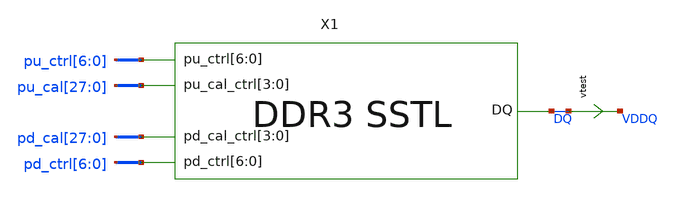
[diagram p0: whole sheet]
** sch_path: schem/sstl_res_tb.sch
* Copyright 2021 Stefan Frederik Schippers
* Licensed under the Apache License, Version 2.0 (the "License");
* you may not use this file except in compliance with the License.
* You may obtain a copy of the License at
* https://www.apache.org/licenses/LICENSE-2.0
* Unless required by applicable law or agreed to in writing, software
* distributed under the License is distributed on an "AS IS" BASIS,
* WITHOUT WARRANTIES OR CONDITIONS OF ANY KIND, either express or implied.
* See the License for the specific language governing permissions and
* limitations under the License.
**.subckt sstl_res_tb
vtest DQ VDDQ 0
.save i(vtest)
X1 DQ pd_ctrl[6] pd_ctrl[5] pd_ctrl[4] pd_ctrl[3] pd_ctrl[2] pd_ctrl[1] pd_ctrl[0] pu_ctrl[6]
+ pu_ctrl[5] pu_ctrl[4] pu_ctrl[3] pu_ctrl[2] pu_ctrl[1] pu_ctrl[0] pd_cal[27] pd_cal[26] pd_cal[25] pd_cal[24]
+ pu_cal[27] pu_cal[26] pu_cal[25] pu_cal[24] SSTL
**** begin user architecture code
 ** Local library links to pdk
.lib ./sky130/libs/SED_process_SED_lib.spice SED_process_SED
.include $::SKYWATER_STDCELLS/sky130_fd_sc_hd.spice

**** end user architecture code
**.ends

* expanding   symbol:  SSTL.sym # of pins=5
** sym_path: schem/SSTL.sym
** sch_path: schem/SSTL.sch
.subckt SSTL DQ pd_ctrl[6] pd_ctrl[5] pd_ctrl[4] pd_ctrl[3] pd_ctrl[2] pd_ctrl[1] pd_ctrl[0]
+ pu_ctrl[6] pu_ctrl[5] pu_ctrl[4] pu_ctrl[3] pu_ctrl[2] pu_ctrl[1] pu_ctrl[0] pd_cal_ctrl[3] pd_cal_ctrl[2]
+ pd_cal_ctrl[1] pd_cal_ctrl[0] pu_cal_ctrl[3] pu_cal_ctrl[2] pu_cal_ctrl[1] pu_cal_ctrl[0]
*.iopin DQ
*.ipin pu_cal_ctrl[3],pu_cal_ctrl[2],pu_cal_ctrl[1],pu_cal_ctrl[0]
*.ipin pd_cal_ctrl[3],pd_cal_ctrl[2],pd_cal_ctrl[1],pd_cal_ctrl[0]
*.ipin pu_ctrl[6],pu_ctrl[5],pu_ctrl[4],pu_ctrl[3],pu_ctrl[2],pu_ctrl[1],pu_ctrl[0]
*.ipin pd_ctrl[6],pd_ctrl[5],pd_ctrl[4],pd_ctrl[3],pd_ctrl[2],pd_ctrl[1],pd_ctrl[0]
X1 DQ n_pu_ctrl[6] n_pu_cal_ctrl[3] n_pu_cal_ctrl[2] n_pu_cal_ctrl[1] n_pu_cal_ctrl[0] p-leg
X2 DQ pd_ctrl_buff[6] pd_cal_ctrl[3] pd_cal_ctrl[2] pd_cal_ctrl[1] pd_cal_ctrl[0] n-leg
X3 DQ n_pu_ctrl[5] n_pu_cal_ctrl[3] n_pu_cal_ctrl[2] n_pu_cal_ctrl[1] n_pu_cal_ctrl[0] p-leg
X4 DQ pd_ctrl_buff[5] pd_cal_ctrl[3] pd_cal_ctrl[2] pd_cal_ctrl[1] pd_cal_ctrl[0] n-leg
X5 DQ n_pu_ctrl[4] n_pu_cal_ctrl[3] n_pu_cal_ctrl[2] n_pu_cal_ctrl[1] n_pu_cal_ctrl[0] p-leg
X6 DQ pd_ctrl_buff[4] pd_cal_ctrl[3] pd_cal_ctrl[2] pd_cal_ctrl[1] pd_cal_ctrl[0] n-leg
X7 DQ n_pu_ctrl[3] n_pu_cal_ctrl[3] n_pu_cal_ctrl[2] n_pu_cal_ctrl[1] n_pu_cal_ctrl[0] p-leg
X8 DQ pd_ctrl_buff[3] pd_cal_ctrl[3] pd_cal_ctrl[2] pd_cal_ctrl[1] pd_cal_ctrl[0] n-leg
X9 DQ n_pu_ctrl[2] n_pu_cal_ctrl[3] n_pu_cal_ctrl[2] n_pu_cal_ctrl[1] n_pu_cal_ctrl[0] p-leg
X10 DQ pd_ctrl_buff[2] pd_cal_ctrl[3] pd_cal_ctrl[2] pd_cal_ctrl[1] pd_cal_ctrl[0] n-leg
X11 DQ n_pu_ctrl[1] n_pu_cal_ctrl[3] n_pu_cal_ctrl[2] n_pu_cal_ctrl[1] n_pu_cal_ctrl[0] p-leg
X12 DQ pd_ctrl_buff[1] pd_cal_ctrl[3] pd_cal_ctrl[2] pd_cal_ctrl[1] pd_cal_ctrl[0] n-leg
X13 DQ n_pu_ctrl[0] n_pu_cal_ctrl[3] n_pu_cal_ctrl[2] n_pu_cal_ctrl[1] n_pu_cal_ctrl[0] p-leg
X14 DQ pd_ctrl_buff[0] pd_cal_ctrl[3] pd_cal_ctrl[2] pd_cal_ctrl[1] pd_cal_ctrl[0] n-leg
xpd_buff_4[6] pdc2[6] VGND VNB VPB VPWR pdc4[6] sky130_fd_sc_hd__clkinv_4
xpd_buff_4[5] pdc2[5] VGND VNB VPB VPWR pdc4[5] sky130_fd_sc_hd__clkinv_4
xpd_buff_4[4] pdc2[4] VGND VNB VPB VPWR pdc4[4] sky130_fd_sc_hd__clkinv_4
xpd_buff_4[3] pdc2[3] VGND VNB VPB VPWR pdc4[3] sky130_fd_sc_hd__clkinv_4
xpd_buff_4[2] pdc2[2] VGND VNB VPB VPWR pdc4[2] sky130_fd_sc_hd__clkinv_4
xpd_buff_4[1] pdc2[1] VGND VNB VPB VPWR pdc4[1] sky130_fd_sc_hd__clkinv_4
xpd_buff_4[0] pdc2[0] VGND VNB VPB VPWR pdc4[0] sky130_fd_sc_hd__clkinv_4
xpd_buff_6[6] pdc4[6] VGND VNB VPB VPWR pd_ctrl_buff[6] sky130_fd_sc_hd__clkbuf_8
xpd_buff_6[5] pdc4[5] VGND VNB VPB VPWR pd_ctrl_buff[5] sky130_fd_sc_hd__clkbuf_8
xpd_buff_6[4] pdc4[4] VGND VNB VPB VPWR pd_ctrl_buff[4] sky130_fd_sc_hd__clkbuf_8
xpd_buff_6[3] pdc4[3] VGND VNB VPB VPWR pd_ctrl_buff[3] sky130_fd_sc_hd__clkbuf_8
xpd_buff_6[2] pdc4[2] VGND VNB VPB VPWR pd_ctrl_buff[2] sky130_fd_sc_hd__clkbuf_8
xpd_buff_6[1] pdc4[1] VGND VNB VPB VPWR pd_ctrl_buff[1] sky130_fd_sc_hd__clkbuf_8
xpd_buff_6[0] pdc4[0] VGND VNB VPB VPWR pd_ctrl_buff[0] sky130_fd_sc_hd__clkbuf_8
xpu_buff_4[6] pu_ctrl[6] VGND VNB VPB VPWR puc4[6] sky130_fd_sc_hd__clkbuf_16
xpu_buff_4[5] pu_ctrl[5] VGND VNB VPB VPWR puc4[5] sky130_fd_sc_hd__clkbuf_16
xpu_buff_4[4] pu_ctrl[4] VGND VNB VPB VPWR puc4[4] sky130_fd_sc_hd__clkbuf_16
xpu_buff_4[3] pu_ctrl[3] VGND VNB VPB VPWR puc4[3] sky130_fd_sc_hd__clkbuf_16
xpu_buff_4[2] pu_ctrl[2] VGND VNB VPB VPWR puc4[2] sky130_fd_sc_hd__clkbuf_16
xpu_buff_4[1] pu_ctrl[1] VGND VNB VPB VPWR puc4[1] sky130_fd_sc_hd__clkbuf_16
xpu_buff_4[0] pu_ctrl[0] VGND VNB VPB VPWR puc4[0] sky130_fd_sc_hd__clkbuf_16
xpu_buff_6[6] puc4[6] VGND VNB VPB VPWR n_pu_ctrl[6] sky130_fd_sc_hd__clkinv_16
xpu_buff_6[5] puc4[5] VGND VNB VPB VPWR n_pu_ctrl[5] sky130_fd_sc_hd__clkinv_16
xpu_buff_6[4] puc4[4] VGND VNB VPB VPWR n_pu_ctrl[4] sky130_fd_sc_hd__clkinv_16
xpu_buff_6[3] puc4[3] VGND VNB VPB VPWR n_pu_ctrl[3] sky130_fd_sc_hd__clkinv_16
xpu_buff_6[2] puc4[2] VGND VNB VPB VPWR n_pu_ctrl[2] sky130_fd_sc_hd__clkinv_16
xpu_buff_6[1] puc4[1] VGND VNB VPB VPWR n_pu_ctrl[1] sky130_fd_sc_hd__clkinv_16
xpu_buff_6[0] puc4[0] VGND VNB VPB VPWR n_pu_ctrl[0] sky130_fd_sc_hd__clkinv_16
xpu_cal_inv[3] pu_cal_ctrl[3] VGND VNB VPB VPWR n_pu_cal_ctrl[3] sky130_fd_sc_hd__inv_1
xpu_cal_inv[2] pu_cal_ctrl[2] VGND VNB VPB VPWR n_pu_cal_ctrl[2] sky130_fd_sc_hd__inv_1
xpu_cal_inv[1] pu_cal_ctrl[1] VGND VNB VPB VPWR n_pu_cal_ctrl[1] sky130_fd_sc_hd__inv_1
xpu_cal_inv[0] pu_cal_ctrl[0] VGND VNB VPB VPWR n_pu_cal_ctrl[0] sky130_fd_sc_hd__inv_1
V1 VDD VPWR 0
V2 VGND GND 0
V3 VDD VPB 0
V4 VNB GND 0
Vpd_ctrl_0 v_pd_ctrl_0 pd_ctrl_buff[6] 0
Vpd_ctrl_1 v_pu_ctrl_0 n_pu_ctrl[6] 0
xpu_buff_2[6] puc4[6] VGND VNB VPB VPWR n_pu_ctrl[6] sky130_fd_sc_hd__clkinv_16
xpu_buff_2[5] puc4[5] VGND VNB VPB VPWR n_pu_ctrl[5] sky130_fd_sc_hd__clkinv_16
xpu_buff_2[4] puc4[4] VGND VNB VPB VPWR n_pu_ctrl[4] sky130_fd_sc_hd__clkinv_16
xpu_buff_2[3] puc4[3] VGND VNB VPB VPWR n_pu_ctrl[3] sky130_fd_sc_hd__clkinv_16
xpu_buff_2[2] puc4[2] VGND VNB VPB VPWR n_pu_ctrl[2] sky130_fd_sc_hd__clkinv_16
xpu_buff_2[1] puc4[1] VGND VNB VPB VPWR n_pu_ctrl[1] sky130_fd_sc_hd__clkinv_16
xpu_buff_2[0] puc4[0] VGND VNB VPB VPWR n_pu_ctrl[0] sky130_fd_sc_hd__clkinv_16
xpd_buff_1[6] pd_ctrl[6] VGND VNB VPB VPWR pdc2[6] sky130_fd_sc_hd__clkinv_4
xpd_buff_1[5] pd_ctrl[5] VGND VNB VPB VPWR pdc2[5] sky130_fd_sc_hd__clkinv_4
xpd_buff_1[4] pd_ctrl[4] VGND VNB VPB VPWR pdc2[4] sky130_fd_sc_hd__clkinv_4
xpd_buff_1[3] pd_ctrl[3] VGND VNB VPB VPWR pdc2[3] sky130_fd_sc_hd__clkinv_4
xpd_buff_1[2] pd_ctrl[2] VGND VNB VPB VPWR pdc2[2] sky130_fd_sc_hd__clkinv_4
xpd_buff_1[1] pd_ctrl[1] VGND VNB VPB VPWR pdc2[1] sky130_fd_sc_hd__clkinv_4
xpd_buff_1[0] pd_ctrl[0] VGND VNB VPB VPWR pdc2[0] sky130_fd_sc_hd__clkinv_4
xpu_buff_1[6] puc4[6] VGND VNB VPB VPWR n_pu_ctrl[6] sky130_fd_sc_hd__clkinv_16
xpu_buff_1[5] puc4[5] VGND VNB VPB VPWR n_pu_ctrl[5] sky130_fd_sc_hd__clkinv_16
xpu_buff_1[4] puc4[4] VGND VNB VPB VPWR n_pu_ctrl[4] sky130_fd_sc_hd__clkinv_16
xpu_buff_1[3] puc4[3] VGND VNB VPB VPWR n_pu_ctrl[3] sky130_fd_sc_hd__clkinv_16
xpu_buff_1[2] puc4[2] VGND VNB VPB VPWR n_pu_ctrl[2] sky130_fd_sc_hd__clkinv_16
xpu_buff_1[1] puc4[1] VGND VNB VPB VPWR n_pu_ctrl[1] sky130_fd_sc_hd__clkinv_16
xpu_buff_1[0] puc4[0] VGND VNB VPB VPWR n_pu_ctrl[0] sky130_fd_sc_hd__clkinv_16
.ends


* expanding   symbol:  p-leg.sym # of pins=3
** sym_path: schem/p-leg.sym
** sch_path: schem/p-leg.sch
.subckt p-leg DQ n_pu_ctrl n_cal_ctrl[3] n_cal_ctrl[2] n_cal_ctrl[1] n_cal_ctrl[0]
*.ipin n_cal_ctrl[3],n_cal_ctrl[2],n_cal_ctrl[1],n_cal_ctrl[0]
*.ipin n_pu_ctrl
*.iopin DQ
XR1 DQ net1 sky130_fd_pr__res_generic_po W=0.33 L=1.8 m=1
XMpullup net1 n_pu_ctrl VDD VDD sky130_fd_pr__pfet_01v8_lvt L=0.35 W=1 nf=1 ad='int((nf+1)/2) * W/nf * 0.29'
+ as='int((nf+2)/2) * W/nf * 0.29' pd='2*int((nf+1)/2) * (W/nf + 0.29)' ps='2*int((nf+2)/2) * (W/nf + 0.29)'
+ nrd='0.29 / W' nrs='0.29 / W' sa=0 sb=0 sd=0 mult=128 m=128
XMctrltot VDD n_cal_ctrl[0] VDD VDD sky130_fd_pr__pfet_01v8_lvt L=0.35 W=1 nf=1 ad='int((nf+1)/2) * W/nf * 0.29'
+ as='int((nf+2)/2) * W/nf * 0.29' pd='2*int((nf+1)/2) * (W/nf + 0.29)' ps='2*int((nf+2)/2) * (W/nf + 0.29)'
+ nrd='0.29 / W' nrs='0.29 / W' sa=0 sb=0 sd=0 mult=120 m=120
XMctrl0 DQ n_cal_ctrl[0] net1 VDD sky130_fd_pr__pfet_01v8_lvt L=0.35 W=1 nf=1 ad='int((nf+1)/2) * W/nf * 0.29'
+ as='int((nf+2)/2) * W/nf * 0.29' pd='2*int((nf+1)/2) * (W/nf + 0.29)' ps='2*int((nf+2)/2) * (W/nf + 0.29)'
+ nrd='0.29 / W' nrs='0.29 / W' sa=0 sb=0 sd=0 mult=48 m=48
XMctrl1 DQ n_cal_ctrl[1] net1 VDD sky130_fd_pr__pfet_01v8_lvt L=0.35 W=1 nf=1 ad='int((nf+1)/2) * W/nf * 0.29'
+ as='int((nf+2)/2) * W/nf * 0.29' pd='2*int((nf+1)/2) * (W/nf + 0.29)' ps='2*int((nf+2)/2) * (W/nf + 0.29)'
+ nrd='0.29 / W' nrs='0.29 / W' sa=0 sb=0 sd=0 mult=16 m=16
XMctrl2 DQ n_cal_ctrl[2] net1 VDD sky130_fd_pr__pfet_01v8_lvt L=0.35 W=1 nf=1 ad='int((nf+1)/2) * W/nf * 0.29'
+ as='int((nf+2)/2) * W/nf * 0.29' pd='2*int((nf+1)/2) * (W/nf + 0.29)' ps='2*int((nf+2)/2) * (W/nf + 0.29)'
+ nrd='0.29 / W' nrs='0.29 / W' sa=0 sb=0 sd=0 mult=8 m=8
XMctrl3 DQ n_cal_ctrl[3] net1 VDD sky130_fd_pr__pfet_01v8_lvt L=0.35 W=1 nf=1 ad='int((nf+1)/2) * W/nf * 0.29'
+ as='int((nf+2)/2) * W/nf * 0.29' pd='2*int((nf+1)/2) * (W/nf + 0.29)' ps='2*int((nf+2)/2) * (W/nf + 0.29)'
+ nrd='0.29 / W' nrs='0.29 / W' sa=0 sb=0 sd=0 mult=4 m=4
.ends


* expanding   symbol:  n-leg.sym # of pins=3
** sym_path: schem/n-leg.sym
** sch_path: schem/n-leg.sch
.subckt n-leg DQ pd_ctrl cal_ctrl[3] cal_ctrl[2] cal_ctrl[1] cal_ctrl[0]
*.iopin DQ
*.ipin pd_ctrl
*.ipin cal_ctrl[3],cal_ctrl[2],cal_ctrl[1],cal_ctrl[0]
XR1 vpulldown DQ sky130_fd_pr__res_generic_po W=0.33 L=1.7 m=1
Xn1 vpulldown pd_ctrl GND GND sky130_fd_pr__nfet_01v8 L=0.15 W=0.65 nf=1 ad='int((nf+1)/2) * W/nf * 0.29'
+ as='int((nf+2)/2) * W/nf * 0.29' pd='2*int((nf+1)/2) * (W/nf + 0.29)' ps='2*int((nf+2)/2) * (W/nf + 0.29)'
+ nrd='0.29 / W' nrs='0.29 / W' sa=0 sb=0 sd=0 mult=48 m=48
Xnctrl0 DQ cal_ctrl[0] vpulldown GND sky130_fd_pr__nfet_01v8 L=0.15 W=0.65 nf=1 ad='int((nf+1)/2) * W/nf * 0.29'
+ as='int((nf+2)/2) * W/nf * 0.29' pd='2*int((nf+1)/2) * (W/nf + 0.29)' ps='2*int((nf+2)/2) * (W/nf + 0.29)'
+ nrd='0.29 / W' nrs='0.29 / W' sa=0 sb=0 sd=0 mult=6 m=6
Xnctrl1 DQ cal_ctrl[1] vpulldown GND sky130_fd_pr__nfet_01v8 L=0.15 W=0.65 nf=1 ad='int((nf+1)/2) * W/nf * 0.29'
+ as='int((nf+2)/2) * W/nf * 0.29' pd='2*int((nf+1)/2) * (W/nf + 0.29)' ps='2*int((nf+2)/2) * (W/nf + 0.29)'
+ nrd='0.29 / W' nrs='0.29 / W' sa=0 sb=0 sd=0 mult=3 m=3
Xnctrl2 DQ cal_ctrl[2] vpulldown GND sky130_fd_pr__nfet_01v8 L=0.15 W=0.975 nf=1 ad='int((nf+1)/2) * W/nf * 0.29'
+ as='int((nf+2)/2) * W/nf * 0.29' pd='2*int((nf+1)/2) * (W/nf + 0.29)' ps='2*int((nf+2)/2) * (W/nf + 0.29)'
+ nrd='0.29 / W' nrs='0.29 / W' sa=0 sb=0 sd=0 mult=1 m=1
Xnctrl3 DQ cal_ctrl[3] vpulldown GND sky130_fd_pr__nfet_01v8 L=0.15 W=0.5 nf=1 ad='int((nf+1)/2) * W/nf * 0.29'
+ as='int((nf+2)/2) * W/nf * 0.29' pd='2*int((nf+1)/2) * (W/nf + 0.29)' ps='2*int((nf+2)/2) * (W/nf + 0.29)'
+ nrd='0.29 / W' nrs='0.29 / W' sa=0 sb=0 sd=0 mult=1 m=1
Xnctrl_tot GND GND GND GND sky130_fd_pr__nfet_01v8 L=0.15 W=0.65 nf=1 ad='int((nf+1)/2) * W/nf * 0.29'
+ as='int((nf+2)/2) * W/nf * 0.29' pd='2*int((nf+1)/2) * (W/nf + 0.29)' ps='2*int((nf+2)/2) * (W/nf + 0.29)'
+ nrd='0.29 / W' nrs='0.29 / W' sa=0 sb=0 sd=0 mult=11 m=11
.ends

.GLOBAL VDD
.GLOBAL GND
**** begin user architecture code


* power voltage
vvddq VDDQ 0 0
vvdd VDD 0 SED_vdd_SED

** CALIBRATION CONTROL **
* PULLUP
vpu_cal00 pu_cal[0] 0 SED_pucal00_SED
vpu_cal01 pu_cal[1] 0 SED_pucal01_SED
vpu_cal02 pu_cal[2] 0 SED_pucal02_SED
vpu_cal03 pu_cal[3] 0 SED_pucal03_SED
vpu_cal10 pu_cal[4] 0 SED_pucal10_SED
vpu_cal11 pu_cal[5] 0 SED_pucal11_SED
vpu_cal12 pu_cal[6] 0 SED_pucal12_SED
vpu_cal13 pu_cal[7] 0 SED_pucal13_SED
vpu_cal20 pu_cal[8] 0 SED_pucal20_SED
vpu_cal21 pu_cal[9] 0 SED_pucal21_SED
vpu_cal22 pu_cal[10] 0 SED_pucal22_SED
vpu_cal23 pu_cal[11] 0 SED_pucal23_SED
vpu_cal30 pu_cal[12] 0 SED_pucal30_SED
vpu_cal31 pu_cal[13] 0 SED_pucal31_SED
vpu_cal32 pu_cal[14] 0 SED_pucal32_SED
vpu_cal33 pu_cal[15] 0 SED_pucal33_SED
vpu_cal40 pu_cal[16] 0 SED_pucal40_SED
vpu_cal41 pu_cal[17] 0 SED_pucal41_SED
vpu_cal42 pu_cal[18] 0 SED_pucal42_SED
vpu_cal43 pu_cal[19] 0 SED_pucal43_SED
vpu_cal50 pu_cal[20] 0 SED_pucal50_SED
vpu_cal51 pu_cal[21] 0 SED_pucal51_SED
vpu_cal52 pu_cal[22] 0 SED_pucal52_SED
vpu_cal53 pu_cal[23] 0 SED_pucal53_SED
vpu_cal60 pu_cal[24] 0 SED_pucal60_SED
vpu_cal61 pu_cal[25] 0 SED_pucal61_SED
vpu_cal62 pu_cal[26] 0 SED_pucal62_SED
vpu_cal63 pu_cal[27] 0 SED_pucal63_SED
* PULLDOWN
vpd_cal00 pd_cal[0] 0 SED_pdcal00_SED
vpd_cal01 pd_cal[1] 0 SED_pdcal01_SED
vpd_cal02 pd_cal[2] 0 SED_pdcal02_SED
vpd_cal03 pd_cal[3] 0 SED_pdcal03_SED
vpd_cal10 pd_cal[4] 0 SED_pdcal10_SED
vpd_cal11 pd_cal[5] 0 SED_pdcal11_SED
vpd_cal12 pd_cal[6] 0 SED_pdcal12_SED
vpd_cal13 pd_cal[7] 0 SED_pdcal13_SED
vpd_cal20 pd_cal[8] 0 SED_pdcal20_SED
vpd_cal21 pd_cal[9] 0 SED_pdcal21_SED
vpd_cal22 pd_cal[10] 0 SED_pdcal22_SED
vpd_cal23 pd_cal[11] 0 SED_pdcal23_SED
vpd_cal30 pd_cal[12] 0 SED_pdcal30_SED
vpd_cal31 pd_cal[13] 0 SED_pdcal31_SED
vpd_cal32 pd_cal[14] 0 SED_pdcal32_SED
vpd_cal33 pd_cal[15] 0 SED_pdcal33_SED
vpd_cal40 pd_cal[16] 0 SED_pdcal40_SED
vpd_cal41 pd_cal[17] 0 SED_pdcal41_SED
vpd_cal42 pd_cal[18] 0 SED_pdcal42_SED
vpd_cal43 pd_cal[19] 0 SED_pdcal43_SED
vpd_cal50 pd_cal[20] 0 SED_pdcal50_SED
vpd_cal51 pd_cal[21] 0 SED_pdcal51_SED
vpd_cal52 pd_cal[22] 0 SED_pdcal52_SED
vpd_cal53 pd_cal[23] 0 SED_pdcal53_SED
vpd_cal60 pd_cal[24] 0 SED_pdcal60_SED
vpd_cal61 pd_cal[25] 0 SED_pdcal61_SED
vpd_cal62 pd_cal[26] 0 SED_pdcal62_SED
vpd_cal63 pd_cal[27] 0 SED_pdcal63_SED

** LEG ENABLE/DISABLE CONTROL
* PULLUP
vpu_ctrl0 pu_ctrl[0] 0 SED_puctrl0_SED
vpu_ctrl1 pu_ctrl[1] 0 SED_puctrl1_SED
vpu_ctrl2 pu_ctrl[2] 0 SED_puctrl2_SED
vpu_ctrl3 pu_ctrl[3] 0 SED_puctrl3_SED
vpu_ctrl4 pu_ctrl[4] 0 SED_puctrl4_SED
vpu_ctrl5 pu_ctrl[5] 0 SED_puctrl5_SED
vpu_ctrl6 pu_ctrl[6] 0 SED_puctrl6_SED
* PULLDOWN
vpd_ctrl0 pd_ctrl[0] 0 SED_pdctrl0_SED
vpd_ctrl1 pd_ctrl[1] 0 SED_pdctrl1_SED
vpd_ctrl2 pd_ctrl[2] 0 SED_pdctrl2_SED
vpd_ctrl3 pd_ctrl[3] 0 SED_pdctrl3_SED
vpd_ctrl4 pd_ctrl[4] 0 SED_pdctrl4_SED
vpd_ctrl5 pd_ctrl[5] 0 SED_pdctrl5_SED
vpd_ctrl6 pd_ctrl[6] 0 SED_pdctrl6_SED


.control
set num_threads=1
save all
set temp=SED_temp_SED

* RUN SIMULATION
dc vvddq 0.3 1.2 0.05
* OUTPUT
print i(vtest)
wrdata out/SED_plotName_SED/SED_plotName_SED.txt i(vtest)
set hcopydevtype = svg
hardcopy ./out/SED_plotName_SED/SED_plotName_SED.svg I(vtest) vs vddq title 'Resistance vs pin voltage'

.endc


**** end user architecture code
.end
